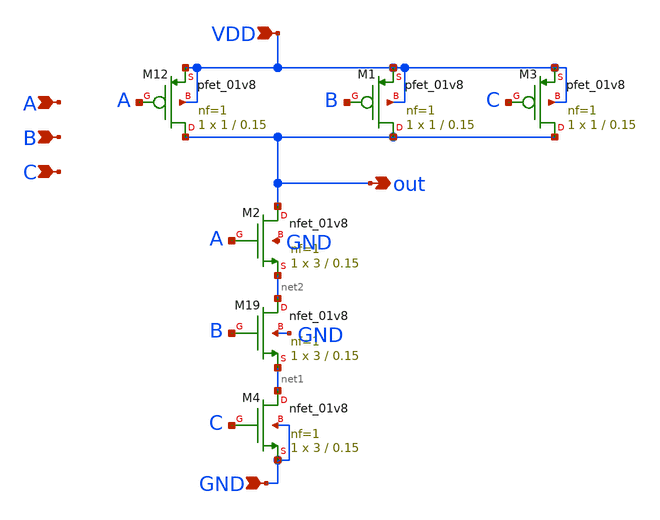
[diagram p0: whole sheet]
** sch_path: xschem/vault/NAND3.sch
**.subckt NAND3 VDD GND out A B C
*.ipin VDD
*.ipin GND
*.opin out
*.ipin A
*.ipin B
*.ipin C
XM12 out A VDD VDD sky130_fd_pr__pfet_01v8 L=0.15 W=1 nf=1 ad='int((nf+1)/2) * W/nf * 0.29' as='int((nf+2)/2) * W/nf * 0.29'
+ pd='2*int((nf+1)/2) * (W/nf + 0.29)' ps='2*int((nf+2)/2) * (W/nf + 0.29)' nrd='0.29 / W' nrs='0.29 / W'
+ sa=0 sb=0 sd=0 mult=1 m=1
XM19 net2 B net1 GND sky130_fd_pr__nfet_01v8 L=0.15 W=3 nf=1 ad='int((nf+1)/2) * W/nf * 0.29' as='int((nf+2)/2) * W/nf * 0.29'
+ pd='2*int((nf+1)/2) * (W/nf + 0.29)' ps='2*int((nf+2)/2) * (W/nf + 0.29)' nrd='0.29 / W' nrs='0.29 / W'
+ sa=0 sb=0 sd=0 mult=1 m=1
XM1 out B VDD VDD sky130_fd_pr__pfet_01v8 L=0.15 W=1 nf=1 ad='int((nf+1)/2) * W/nf * 0.29' as='int((nf+2)/2) * W/nf * 0.29'
+ pd='2*int((nf+1)/2) * (W/nf + 0.29)' ps='2*int((nf+2)/2) * (W/nf + 0.29)' nrd='0.29 / W' nrs='0.29 / W'
+ sa=0 sb=0 sd=0 mult=1 m=1
XM2 out A net2 GND sky130_fd_pr__nfet_01v8 L=0.15 W=3 nf=1 ad='int((nf+1)/2) * W/nf * 0.29' as='int((nf+2)/2) * W/nf * 0.29'
+ pd='2*int((nf+1)/2) * (W/nf + 0.29)' ps='2*int((nf+2)/2) * (W/nf + 0.29)' nrd='0.29 / W' nrs='0.29 / W'
+ sa=0 sb=0 sd=0 mult=1 m=1
XM3 out C VDD VDD sky130_fd_pr__pfet_01v8 L=0.15 W=1 nf=1 ad='int((nf+1)/2) * W/nf * 0.29' as='int((nf+2)/2) * W/nf * 0.29'
+ pd='2*int((nf+1)/2) * (W/nf + 0.29)' ps='2*int((nf+2)/2) * (W/nf + 0.29)' nrd='0.29 / W' nrs='0.29 / W'
+ sa=0 sb=0 sd=0 mult=1 m=1
XM4 net1 C GND GND sky130_fd_pr__nfet_01v8 L=0.15 W=3 nf=1 ad='int((nf+1)/2) * W/nf * 0.29' as='int((nf+2)/2) * W/nf * 0.29'
+ pd='2*int((nf+1)/2) * (W/nf + 0.29)' ps='2*int((nf+2)/2) * (W/nf + 0.29)' nrd='0.29 / W' nrs='0.29 / W'
+ sa=0 sb=0 sd=0 mult=1 m=1
**.ends
.end
